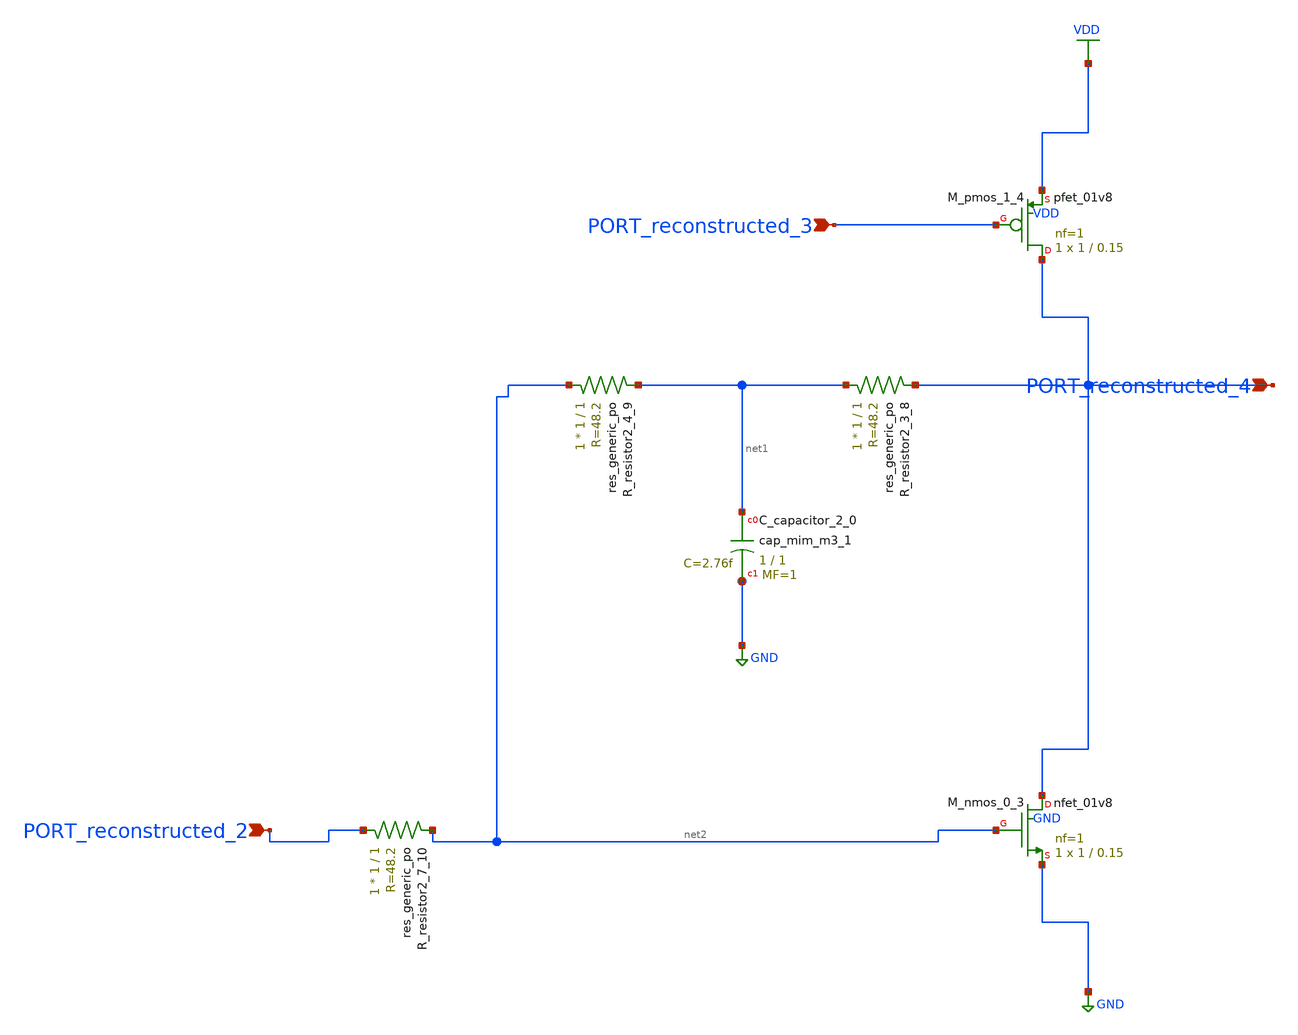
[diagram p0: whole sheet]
** sch_path: schematics/AMSNet/622.sch
**.subckt 622 PORT_reconstructed_2 PORT_reconstructed_3 PORT_reconstructed_4
*.ipin PORT_reconstructed_2
*.ipin PORT_reconstructed_3
*.ipin PORT_reconstructed_4
XC_capacitor_2_0 net1 GND sky130_fd_pr__cap_mim_m3_1 W=1 L=1 MF=1 m=1
XM_nmos_0_3 PORT_reconstructed_4 net2 GND GND sky130_fd_pr__nfet_01v8 L=0.15 W=1 nf=1 ad='int((1 + 1)/2) * 1 / 1 * 0.29'
+ as='int((1 + 2)/2) * 1 / 1 * 0.29' pd='2*int((1 + 1)/2) * (1 / 1 + 0.29)' ps='2*int((1 + 2)/2) * (1 / 1 + 0.29)'
+ nrd='0.29 / 1 ' nrs='0.29 / 1 ' sa=0 sb=0 sd=0 mult=1 m=1
XM_pmos_1_4 PORT_reconstructed_4 PORT_reconstructed_3 VDD VDD sky130_fd_pr__pfet_01v8 L=0.15 W=1 nf=1
+ ad='int((1 + 1)/2) * 1 / 1 * 0.29' as='int((1 + 2)/2) * 1 / 1 * 0.29' pd='2*int((1 + 1)/2) * (1 / 1 + 0.29)'
+ ps='2*int((1 + 2)/2) * (1 / 1 + 0.29)' nrd='0.29 / 1 ' nrs='0.29 / 1 ' sa=0 sb=0 sd=0 mult=1 m=1
XR_resistor2_3_8 net1 PORT_reconstructed_4 sky130_fd_pr__res_generic_po W=1 L=1 m=1
XR_resistor2_4_9 net2 net1 sky130_fd_pr__res_generic_po W=1 L=1 m=1
XR_resistor2_7_10 PORT_reconstructed_2 net2 sky130_fd_pr__res_generic_po W=1 L=1 m=1
**.ends
.GLOBAL GND
.GLOBAL VDD
.end
